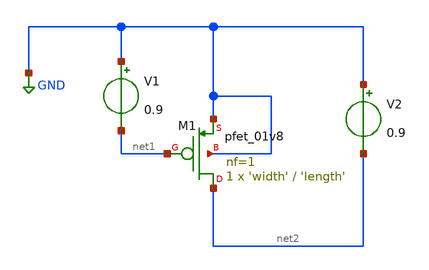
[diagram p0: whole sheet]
** sch_path: PMOS_Charac/pmos_gmid.sch
**.subckt pmos_gmid
XM1 net2 net1 GND GND sky130_fd_pr__pfet_01v8 L='length' W='width' nf=1 ad='int((nf+1)/2) * W/nf * 0.29'
+ as='int((nf+2)/2) * W/nf * 0.29' pd='2*int((nf+1)/2) * (W/nf + 0.29)' ps='2*int((nf+2)/2) * (W/nf + 0.29)'
+ nrd='0.29 / W' nrs='0.29 / W' sa=0 sb=0 sd=0 mult=1 m=1
V1 GND net1 0.9
V2 GND net2 0.9
**** begin user architecture code



.lib /usr/local/share/pdk/sky130A/libs.tech/ngspice/sky130.lib.spice tt
.option wnflag=1

.param length = 0.4
.param width = 1

.control
save all

save @m.xm1.msky130_fd_pr__pfet_01v8[gm]
save @m.xm1.msky130_fd_pr__pfet_01v8[id]
save @m.xm1.msky130_fd_pr__pfet_01v8[gds]
save @m.xm1.msky130_fd_pr__pfet_01v8[cgg]
save @m.xm1.msky130_fd_pr__pfet_01v8[vdsat]
save @m.xm1.msky130_fd_pr__pfet_01v8[vgs]

dc v1 0 1 1m

let gm = @m.xm1.msky130_fd_pr__pfet_01v8[gm]
let id = @m.xm1.msky130_fd_pr__pfet_01v8[id]
let gds = @m.xm1.msky130_fd_pr__pfet_01v8[gds]
let cgg = @m.xm1.msky130_fd_pr__pfet_01v8[cgg]
let vdsat = @m.xm1.msky130_fd_pr__pfet_01v8[vdsat]
let vgs = @m.xm1.msky130_fd_pr__pfet_01v8[vgs]

let gmro = gm/gds
let ft = gm/(2*pi*cgg)
let gmoverid = gm/id

wrdata gmro.txt gmro
wrdata ft.txt ft
wrdata gmoverid.txt gmoverid
wrdata id.txt id
wrdata vdsat.txt vdsat
wrdata vgs.txt vgs

.endc




**** end user architecture code
**.ends
.GLOBAL GND
.end
